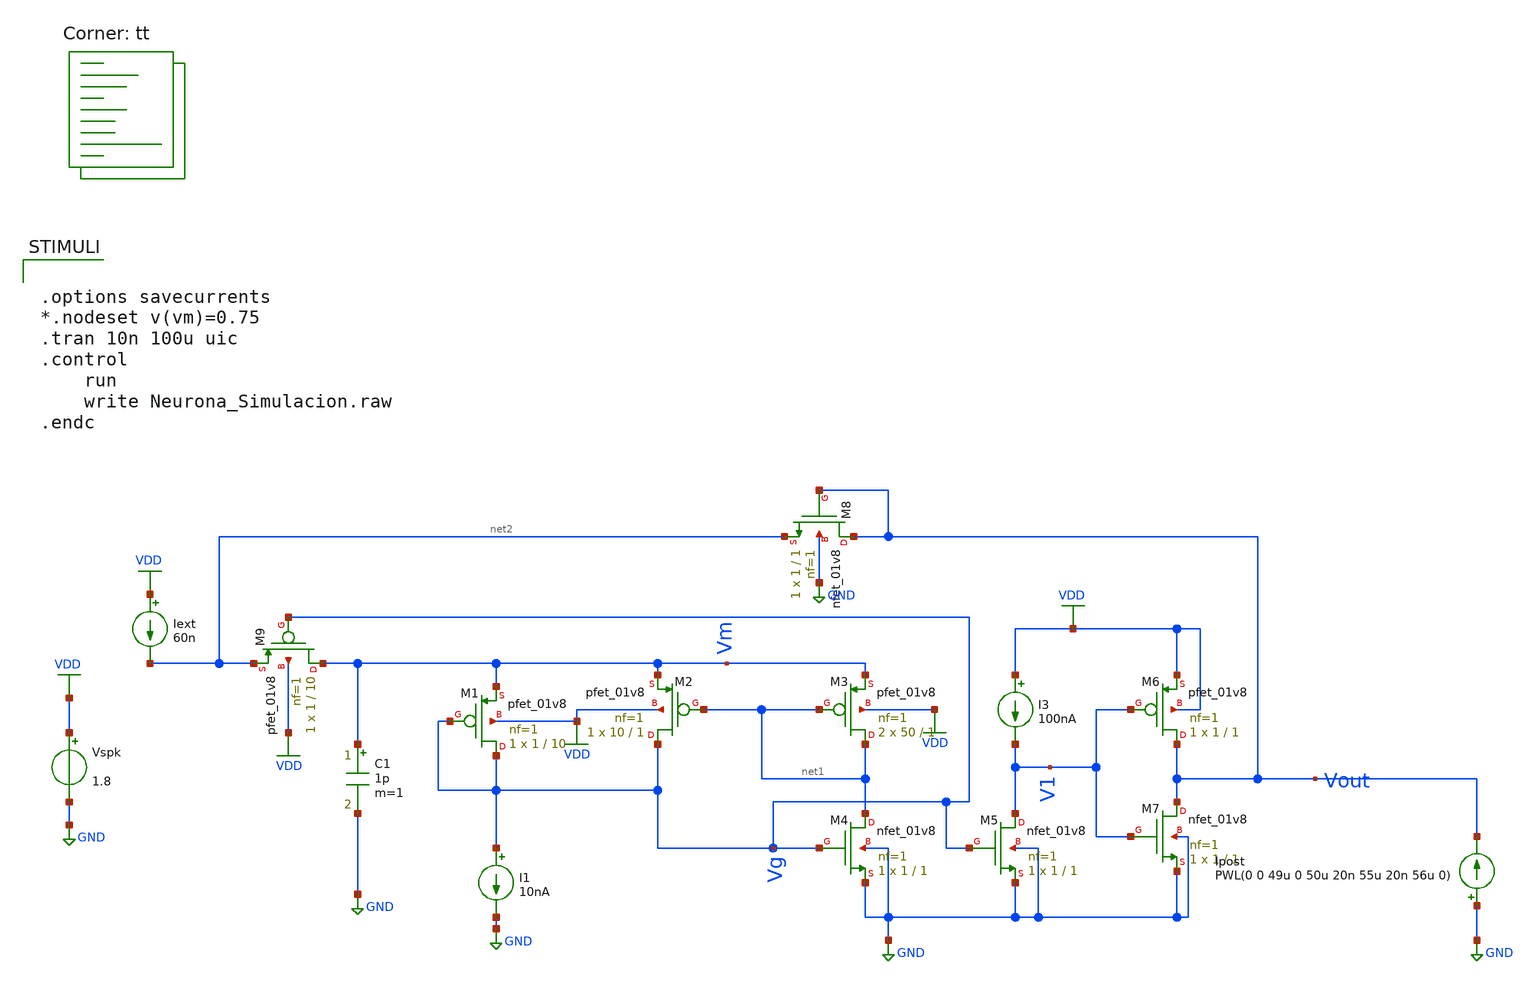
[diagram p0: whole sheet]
** sch_path: Neuron/ultralif/Neurona_Simulacion.sch
**.subckt Neurona_Simulacion
XM1 Vg Vg Vm VDD sky130_fd_pr__pfet_01v8 L=10 W=1 nf=1 ad='int((nf+1)/2) * W/nf * 0.29' as='int((nf+2)/2) * W/nf * 0.29'
+ pd='2*int((nf+1)/2) * (W/nf + 0.29)' ps='2*int((nf+2)/2) * (W/nf + 0.29)' nrd='0.29 / W' nrs='0.29 / W'
+ sa=0 sb=0 sd=0 mult=1 m=1
XM2 Vg net1 Vm VDD sky130_fd_pr__pfet_01v8 L=1 W=10 nf=1 ad='int((nf+1)/2) * W/nf * 0.29' as='int((nf+2)/2) * W/nf * 0.29'
+ pd='2*int((nf+1)/2) * (W/nf + 0.29)' ps='2*int((nf+2)/2) * (W/nf + 0.29)' nrd='0.29 / W' nrs='0.29 / W'
+ sa=0 sb=0 sd=0 mult=1 m=1
XM3 net1 net1 Vm VDD sky130_fd_pr__pfet_01v8 L=1 W=50 nf=1 ad='int((nf+1)/2) * W/nf * 0.29' as='int((nf+2)/2) * W/nf * 0.29'
+ pd='2*int((nf+1)/2) * (W/nf + 0.29)' ps='2*int((nf+2)/2) * (W/nf + 0.29)' nrd='0.29 / W' nrs='0.29 / W'
+ sa=0 sb=0 sd=0 mult=2 m=2
XM4 net1 Vg GND GND sky130_fd_pr__nfet_01v8 L=1 W=1 nf=1 ad='int((1 + 1)/2) * 1 / 1 * 0.29' as='int((1 + 2)/2) * 1 / 1 * 0.29'
+ pd='2*int((1 + 1)/2) * (1 / 1 + 0.29)' ps='2*int((1 + 2)/2) * (1 / 1 + 0.29)' nrd='0.29 / 1 ' nrs='0.29 / 1 '
+ sa=0 sb=0 sd=0 mult=1 m=1
XM5 V1 Vg GND GND sky130_fd_pr__nfet_01v8 L=1 W=1 nf=1 ad='int((1 + 1)/2) * 1 / 1 * 0.29' as='int((1 + 2)/2) * 1 / 1 * 0.29'
+ pd='2*int((1 + 1)/2) * (1 / 1 + 0.29)' ps='2*int((1 + 2)/2) * (1 / 1 + 0.29)' nrd='0.29 / 1 ' nrs='0.29 / 1 '
+ sa=0 sb=0 sd=0 mult=1 m=1
XM6 Vout V1 VDD VDD sky130_fd_pr__pfet_01v8 L=1 W=1 nf=1 ad='int((nf+1)/2) * W/nf * 0.29' as='int((nf+2)/2) * W/nf * 0.29'
+ pd='2*int((nf+1)/2) * (W/nf + 0.29)' ps='2*int((nf+2)/2) * (W/nf + 0.29)' nrd='0.29 / W' nrs='0.29 / W'
+ sa=0 sb=0 sd=0 mult=1 m=1
XM7 Vout V1 GND GND sky130_fd_pr__nfet_01v8 L=1 W=1 nf=1 ad='int((1 + 1)/2) * 1 / 1 * 0.29' as='int((1 + 2)/2) * 1 / 1 * 0.29'
+ pd='2*int((1 + 1)/2) * (1 / 1 + 0.29)' ps='2*int((1 + 2)/2) * (1 / 1 + 0.29)' nrd='0.29 / 1 ' nrs='0.29 / 1 '
+ sa=0 sb=0 sd=0 mult=1 m=1
I1 Vg GND 10nA
Vspk VDD GND 1.8
C1 Vm GND 1p m=1
Iext VDD net2 60n
I3 VDD V1 100nA
XM8 Vout Vout net2 GND sky130_fd_pr__nfet_01v8 L=1 W=1 nf=1 ad='int((1 + 1)/2) * 1 / 1 * 0.29' as='int((1 + 2)/2) * 1 / 1 * 0.29'
+ pd='2*int((1 + 1)/2) * (1 / 1 + 0.29)' ps='2*int((1 + 2)/2) * (1 / 1 + 0.29)' nrd='0.29 / 1 ' nrs='0.29 / 1 '
+ sa=0 sb=0 sd=0 mult=1 m=1
XM9 Vm Vg net2 VDD sky130_fd_pr__pfet_01v8 L=10 W=1 nf=1 ad='int((nf+1)/2) * W/nf * 0.29' as='int((nf+2)/2) * W/nf * 0.29'
+ pd='2*int((nf+1)/2) * (W/nf + 0.29)' ps='2*int((nf+2)/2) * (W/nf + 0.29)' nrd='0.29 / W' nrs='0.29 / W'
+ sa=0 sb=0 sd=0 mult=1 m=1
Ipost GND Vout PWL(0 0 49u 0 50u 20n 55u 20n 56u 0)
**** begin user architecture code
.lib $::SKYWATER_MODELS/sky130.lib.spice tt
**** end user architecture code
**.ends
.GLOBAL GND
.GLOBAL VDD
**** begin user architecture code


.options savecurrents
*.nodeset v(vm)=0.75
.tran 10n 100u uic
.control
	run
	write Neurona_Simulacion.raw
.endc


**** end user architecture code
.end
